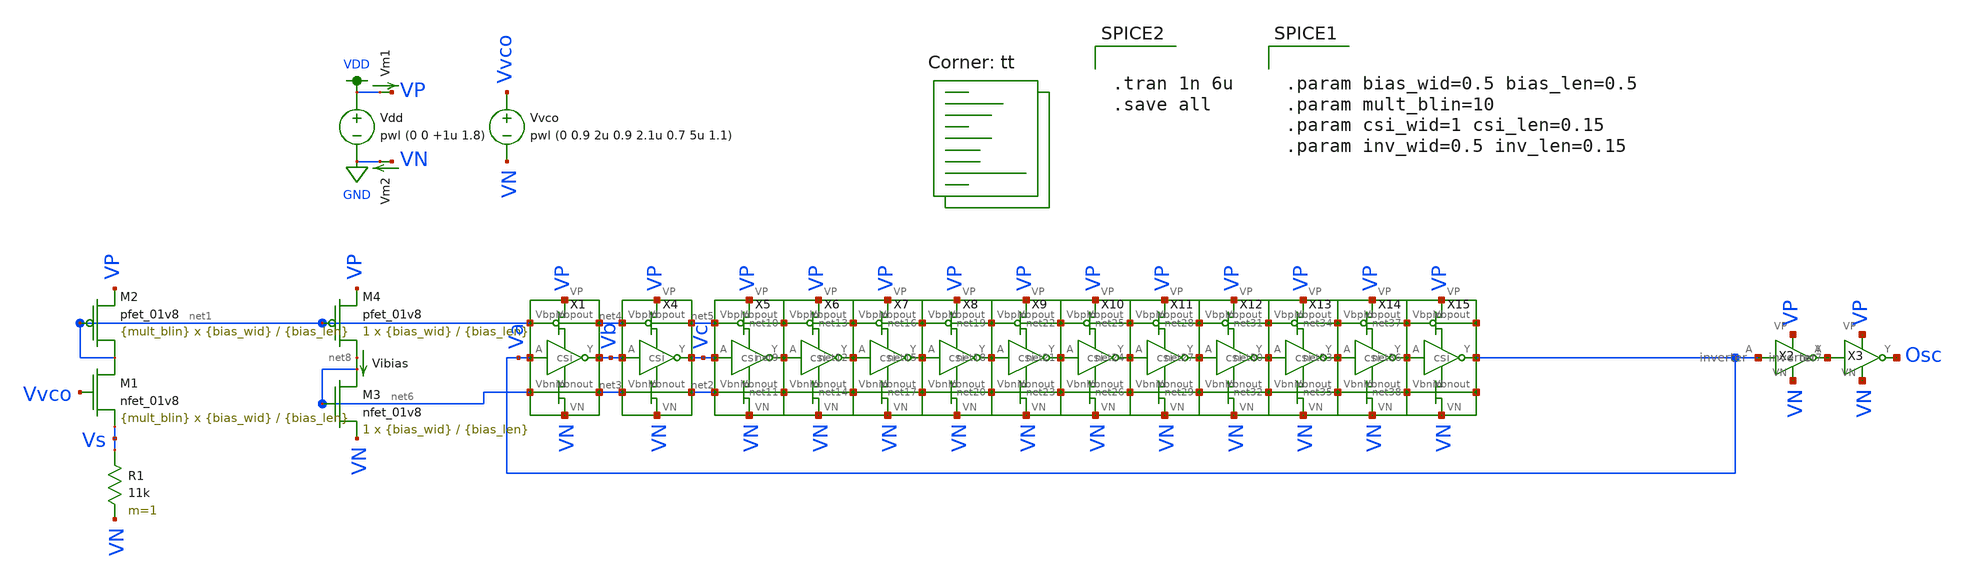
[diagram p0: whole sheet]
** sch_path: test_vco_sweep.sch
**.subckt test_vco_sweep
X1 VP VN Va Vb net1 net6 net4 net3 csi
X2 Va net7 VP VN inverter
X3 net7 Osc VP VN inverter
XM3 net6 net6 VN VN sky130_fd_pr__nfet_01v8 L={bias_len} W={bias_wid} nf=1 ad='int((nf+1)/2) * W/nf * 0.29'
+ as='int((nf+2)/2) * W/nf * 0.29' pd='2*int((nf+1)/2) * (W/nf + 0.29)' ps='2*int((nf+2)/2) * (W/nf + 0.29)'
+ nrd='0.29 / W' nrs='0.29 / W' sa=0 sb=0 sd=0 mult=1 m=1
XM4 net8 net1 VP VP sky130_fd_pr__pfet_01v8 L={bias_len} W={bias_wid} nf=1 ad='int((nf+1)/2) * W/nf * 0.29'
+ as='int((nf+2)/2) * W/nf * 0.29' pd='2*int((nf+1)/2) * (W/nf + 0.29)' ps='2*int((nf+2)/2) * (W/nf + 0.29)'
+ nrd='0.29 / W' nrs='0.29 / W' sa=0 sb=0 sd=0 mult=1 m=1
X4 VP VN Vb Vc net4 net3 net5 net2 csi
X5 VP VN Vc net9 net5 net2 net10 net11 csi
Vdd VDD GND pwl (0 0 +1u 1.8)
Vm1 VDD VP 0
.save i(vm1)
Vm2 VN GND 0
.save i(vm2)
Vvco Vvco VN pwl (0 0.9 2u 0.9 2.1u 0.7 5u 1.1)
X6 VP VN net9 net12 net10 net11 net13 net14 csi
X7 VP VN net12 net15 net13 net14 net16 net17 csi
X8 VP VN net15 net18 net16 net17 net19 net20 csi
X9 VP VN net18 net21 net19 net20 net22 net23 csi
R1 Vs VN 11k m=1
XM1 net1 Vvco Vs VN sky130_fd_pr__nfet_01v8 L={bias_len} W={bias_wid} nf=1 ad='int((nf+1)/2) * W/nf * 0.29'
+ as='int((nf+2)/2) * W/nf * 0.29' pd='2*int((nf+1)/2) * (W/nf + 0.29)' ps='2*int((nf+2)/2) * (W/nf + 0.29)'
+ nrd='0.29 / W' nrs='0.29 / W' sa=0 sb=0 sd=0 mult={mult_blin} m={mult_blin}
XM2 net1 net1 VP VP sky130_fd_pr__pfet_01v8 L={bias_len} W={bias_wid} nf=1 ad='int((nf+1)/2) * W/nf * 0.29'
+ as='int((nf+2)/2) * W/nf * 0.29' pd='2*int((nf+1)/2) * (W/nf + 0.29)' ps='2*int((nf+2)/2) * (W/nf + 0.29)'
+ nrd='0.29 / W' nrs='0.29 / W' sa=0 sb=0 sd=0 mult={mult_blin} m={mult_blin}
Vibias net8 net6 0
.save i(vibias)
X10 VP VN net21 net24 net22 net23 net25 net26 csi
X11 VP VN net24 net27 net25 net26 net28 net29 csi
X12 VP VN net27 net30 net28 net29 net31 net32 csi
X13 VP VN net30 net33 net31 net32 net34 net35 csi
X14 VP VN net33 net36 net34 net35 net37 net38 csi
X15 VP VN net36 Va net37 net38 net39 net40 csi
**** begin user architecture code


.tran 1n 6u
.save all




.param bias_wid=0.5 bias_len=0.5
.param mult_blin=10
.param csi_wid=1 csi_len=0.15
.param inv_wid=0.5 inv_len=0.15


.lib $::SKYWATER_MODELS/sky130.lib.spice tt
**** end user architecture code
**.ends

* expanding   symbol:  csi.sym # of pins=8
** sym_path: csi.sym
** sch_path: csi.sch
.subckt csi VP VN A Y Vbpin Vbnin Vbpout Vbnout
*.iopin VN
*.iopin VP
*.opin Y
*.ipin Vbpin
*.ipin A
*.ipin Vbnin
*.opin Vbpout
*.opin Vbnout
XM1 Y A net1 VN sky130_fd_pr__nfet_01v8 L={csi_len} W={csi_wid} nf=1 ad='int((nf+1)/2) * W/nf * 0.29'
+ as='int((nf+2)/2) * W/nf * 0.29' pd='2*int((nf+1)/2) * (W/nf + 0.29)' ps='2*int((nf+2)/2) * (W/nf + 0.29)'
+ nrd='0.29 / W' nrs='0.29 / W' sa=0 sb=0 sd=0 mult=1 m=1
XM2 Y A net2 VP sky130_fd_pr__pfet_01v8 L={csi_len} W={csi_wid} nf=1 ad='int((nf+1)/2) * W/nf * 0.29'
+ as='int((nf+2)/2) * W/nf * 0.29' pd='2*int((nf+1)/2) * (W/nf + 0.29)' ps='2*int((nf+2)/2) * (W/nf + 0.29)'
+ nrd='0.29 / W' nrs='0.29 / W' sa=0 sb=0 sd=0 mult=1 m=1
XM3 net1 Vbnin VN VN sky130_fd_pr__nfet_01v8 L={bias_len} W={bias_wid} nf=1 ad='int((nf+1)/2) * W/nf * 0.29'
+ as='int((nf+2)/2) * W/nf * 0.29' pd='2*int((nf+1)/2) * (W/nf + 0.29)' ps='2*int((nf+2)/2) * (W/nf + 0.29)'
+ nrd='0.29 / W' nrs='0.29 / W' sa=0 sb=0 sd=0 mult=1 m=1
XM4 net2 Vbpin VP VP sky130_fd_pr__pfet_01v8 L={bias_len} W={bias_wid} nf=1 ad='int((nf+1)/2) * W/nf * 0.29'
+ as='int((nf+2)/2) * W/nf * 0.29' pd='2*int((nf+1)/2) * (W/nf + 0.29)' ps='2*int((nf+2)/2) * (W/nf + 0.29)'
+ nrd='0.29 / W' nrs='0.29 / W' sa=0 sb=0 sd=0 mult=1 m=1
Vm1 Vbpin Vbpout 0
.save i(vm1)
Vm2 Vbnin Vbnout 0
.save i(vm2)
.ends


* expanding   symbol:  inverter.sym # of pins=4
** sym_path: inverter.sym
** sch_path: inverter.sch
.subckt inverter A Y VP VN
*.iopin VP
*.ipin A
*.opin Y
*.iopin VN
XM2 Y A VP VP sky130_fd_pr__pfet_01v8 L={inv_len} W={inv_wid} nf=1 ad='int((nf+1)/2) * W/nf * 0.29' as='int((nf+2)/2) * W/nf * 0.29'
+ pd='2*int((nf+1)/2) * (W/nf + 0.29)' ps='2*int((nf+2)/2) * (W/nf + 0.29)' nrd='0.29 / W' nrs='0.29 / W'
+ sa=0 sb=0 sd=0 mult=1 m=1
XM1 Y A VN VN sky130_fd_pr__nfet_01v8 L={inv_len} W={inv_wid} nf=1 ad='int((nf+1)/2) * W/nf * 0.29' as='int((nf+2)/2) * W/nf * 0.29'
+ pd='2*int((nf+1)/2) * (W/nf + 0.29)' ps='2*int((nf+2)/2) * (W/nf + 0.29)' nrd='0.29 / W' nrs='0.29 / W'
+ sa=0 sb=0 sd=0 mult=1 m=1
.ends

.GLOBAL GND
.GLOBAL VDD
.end
